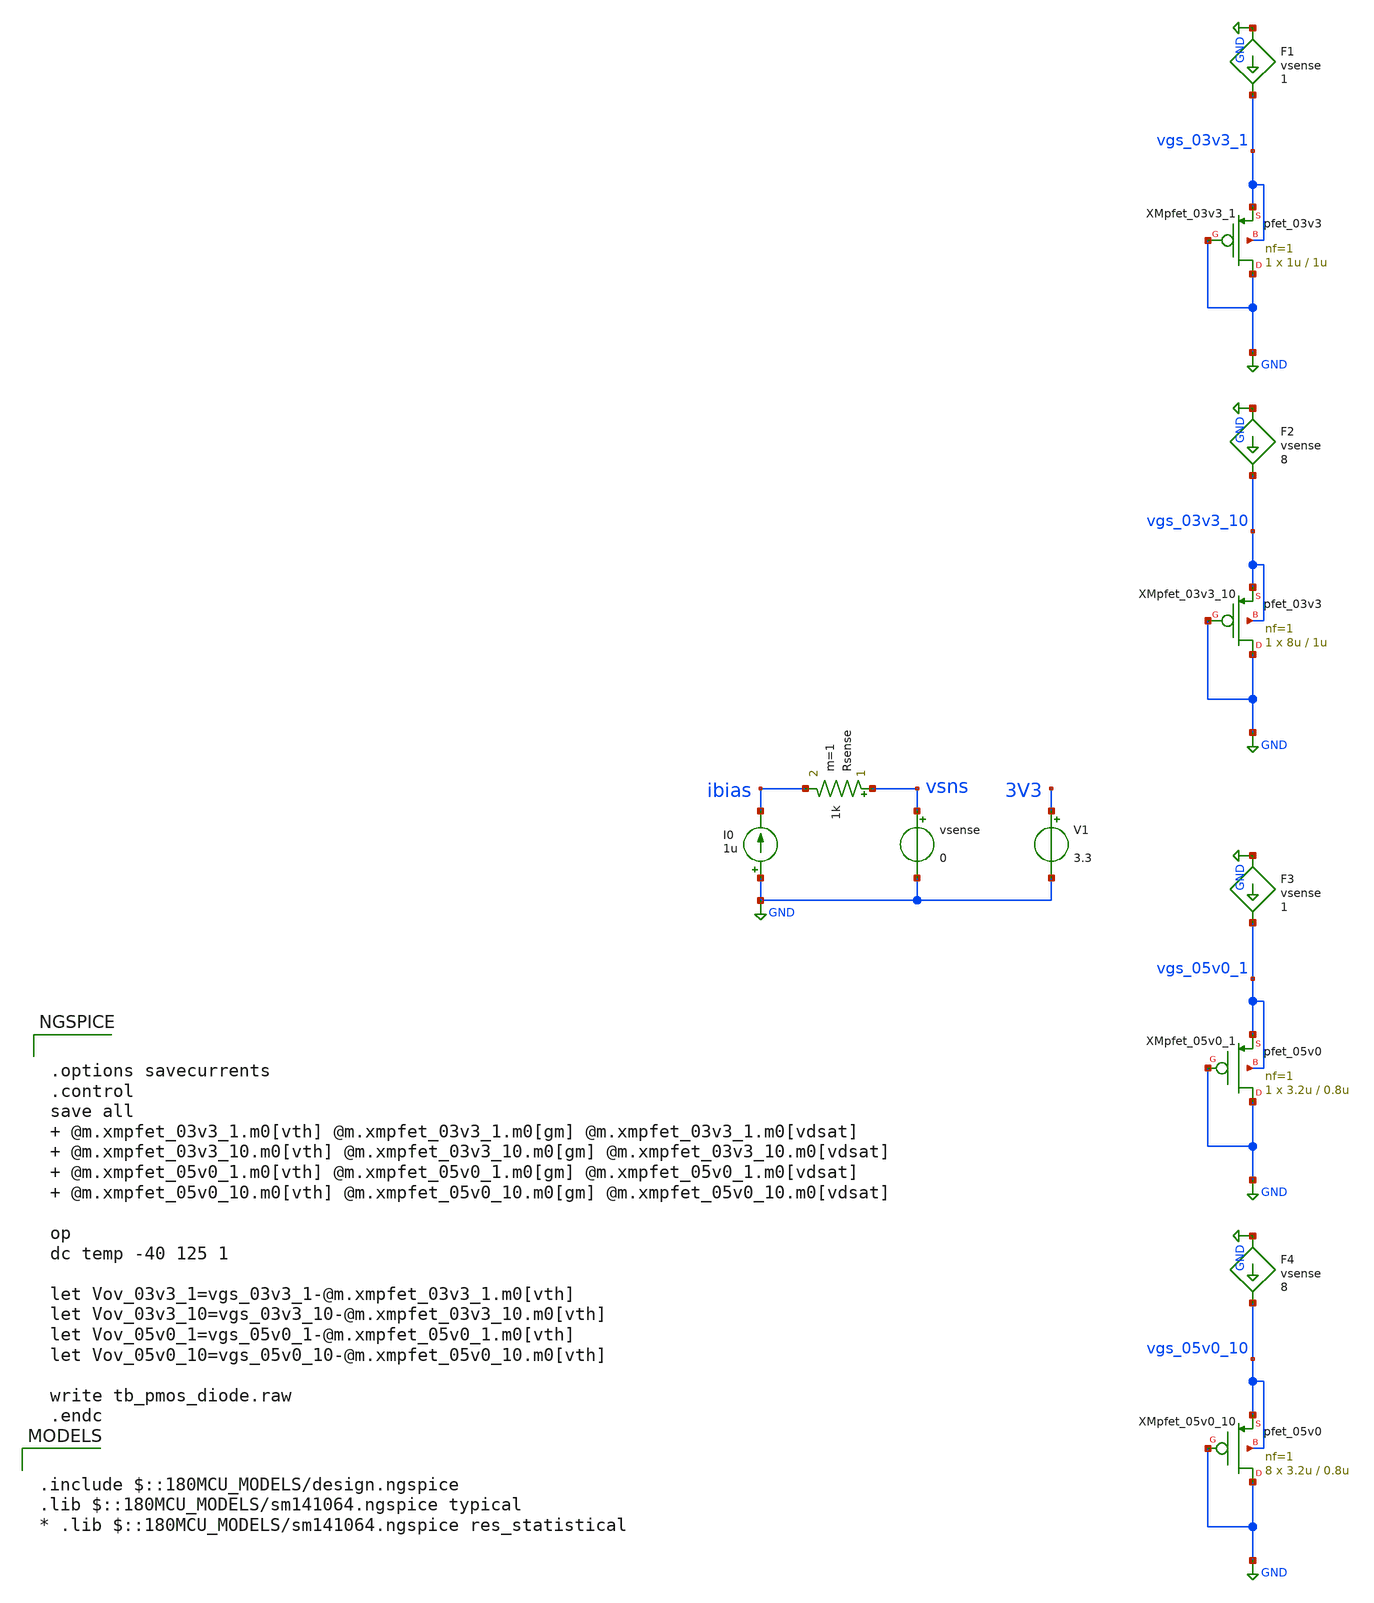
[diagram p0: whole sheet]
** sch_path: designs/libs/tb_analog/tb_pmos_diode/tb_pmos_diode.sch
**.subckt tb_pmos_diode
I0 GND ibias 1u
Rsense vsns ibias 1k m=1
vsense vsns GND 0
V1 3V3 GND 3.3
F1 GND vgs_03v3_1 vsense 1
F2 GND vgs_03v3_10 vsense 8
F3 GND vgs_05v0_1 vsense 1
F4 GND vgs_05v0_10 vsense 8
XMpfet_03v3_1 GND GND vgs_03v3_1 vgs_03v3_1 pfet_03v3 L=1u W=1u nf=1 ad='int((nf+1)/2) * W/nf * 0.18u'
+ as='int((nf+2)/2) * W/nf * 0.18u' pd='2*int((nf+1)/2) * (W/nf + 0.18u)' ps='2*int((nf+2)/2) * (W/nf + 0.18u)'
+ nrd='0.18u / W' nrs='0.18u / W' sa=0 sb=0 sd=0 m=1
XMpfet_03v3_10 GND GND vgs_03v3_10 vgs_03v3_10 pfet_03v3 L=1u W=8u nf=1 ad='int((nf+1)/2) * W/nf * 0.18u'
+ as='int((nf+2)/2) * W/nf * 0.18u' pd='2*int((nf+1)/2) * (W/nf + 0.18u)' ps='2*int((nf+2)/2) * (W/nf + 0.18u)'
+ nrd='0.18u / W' nrs='0.18u / W' sa=0 sb=0 sd=0 m=1
XMpfet_05v0_1 GND GND vgs_05v0_1 vgs_05v0_1 pfet_05v0 L=0.8u W=3.2u nf=1 ad='int((nf+1)/2) * W/nf * 0.18u'
+ as='int((nf+2)/2) * W/nf * 0.18u' pd='2*int((nf+1)/2) * (W/nf + 0.18u)' ps='2*int((nf+2)/2) * (W/nf + 0.18u)'
+ nrd='0.18u / W' nrs='0.18u / W' sa=0 sb=0 sd=0 m=1
XMpfet_05v0_10 GND GND vgs_05v0_10 vgs_05v0_10 pfet_05v0 L=0.8u W=3.2u nf=1 ad='int((nf+1)/2) * W/nf * 0.18u'
+ as='int((nf+2)/2) * W/nf * 0.18u' pd='2*int((nf+1)/2) * (W/nf + 0.18u)' ps='2*int((nf+2)/2) * (W/nf + 0.18u)'
+ nrd='0.18u / W' nrs='0.18u / W' sa=0 sb=0 sd=0 m=8
**** begin user architecture code

.include $::180MCU_MODELS/design.ngspice
.lib $::180MCU_MODELS/sm141064.ngspice typical
* .lib $::180MCU_MODELS/sm141064.ngspice res_statistical



.options savecurrents
.control
save all   @m.xmpfet_03v3_1.m0[vth] @m.xmpfet_03v3_1.m0[gm] @m.xmpfet_03v3_1.m0[vdsat]
+  @m.xmpfet_03v3_10.m0[vth] @m.xmpfet_03v3_10.m0[gm] @m.xmpfet_03v3_10.m0[vdsat]  @m.xmpfet_05v0_1.m0[vth]
+ @m.xmpfet_05v0_1.m0[gm] @m.xmpfet_05v0_1.m0[vdsat]  @m.xmpfet_05v0_10.m0[vth] @m.xmpfet_05v0_10.m0[gm]
+ @m.xmpfet_05v0_10.m0[vdsat]

op
dc temp -40 125 1

let Vov_03v3_1=vgs_03v3_1-@m.xmpfet_03v3_1.m0[vth]
let Vov_03v3_10=vgs_03v3_10-@m.xmpfet_03v3_10.m0[vth]
let Vov_05v0_1=vgs_05v0_1-@m.xmpfet_05v0_1.m0[vth]
let Vov_05v0_10=vgs_05v0_10-@m.xmpfet_05v0_10.m0[vth]

write tb_pmos_diode.raw
.endc


**** end user architecture code
**.ends
.GLOBAL GND
.end
